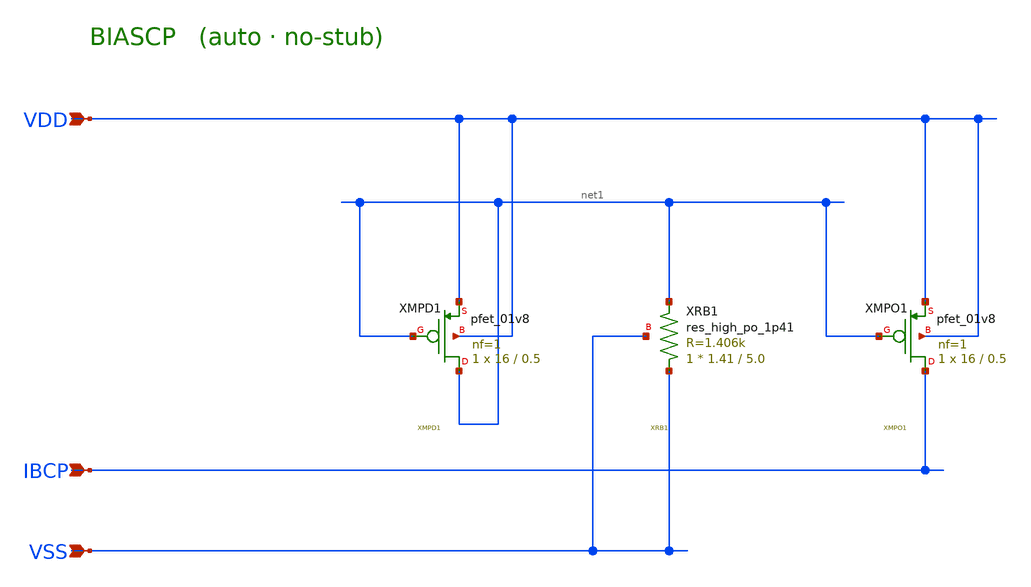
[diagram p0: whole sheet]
** sch_path: schematics/BIASCP.sch
**.subckt BIASCP VDD VSS IBCP
*.ipin VDD
*.ipin VSS
*.ipin IBCP
XXMPD1 net1 net1 VDD VDD sky130_fd_pr__pfet_01v8 L=0.5 W=16 nf=1 ad='int((nf+1)/2) * W/nf * 0.29' as='int((nf+2)/2) * W/nf * 0.29'
+ pd='2*int((nf+1)/2) * (W/nf + 0.29)' ps='2*int((nf+2)/2) * (W/nf + 0.29)' nrd='0.29 / W' nrs='0.29 / W'
+ sa=0 sb=0 sd=0 mult=1 m=1
XXRB1 VSS net1 VSS sky130_fd_pr__res_high_po_1p41 L=5.0 mult=1 m=1
XXMPO1 IBCP net1 VDD VDD sky130_fd_pr__pfet_01v8 L=0.5 W=16 nf=1 ad='int((nf+1)/2) * W/nf * 0.29' as='int((nf+2)/2) * W/nf * 0.29'
+ pd='2*int((nf+1)/2) * (W/nf + 0.29)' ps='2*int((nf+2)/2) * (W/nf + 0.29)' nrd='0.29 / W' nrs='0.29 / W'
+ sa=0 sb=0 sd=0 mult=1 m=1
**.ends
.end
